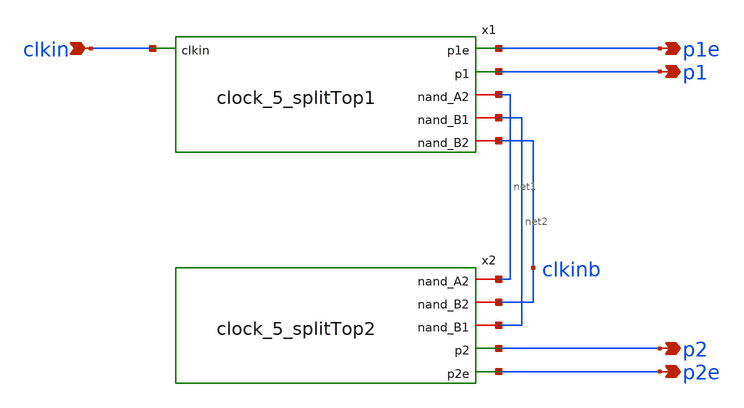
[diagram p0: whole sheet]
** sch_path: 5_Design/4_Layout/Team 5/xschem/clock_5_splitTop.sch
**.subckt clock_5_splitTop clkin p1e p1 p2 p2e
*.ipin clkin
*.opin p1e
*.opin p1
*.opin p2
*.opin p2e
x1 p1e clkin p1 net1 net2 clkinb clock_5_splitTop1
x2 net1 clkinb net2 p2 p2e clock_5_splitTop2
**.ends
.end
